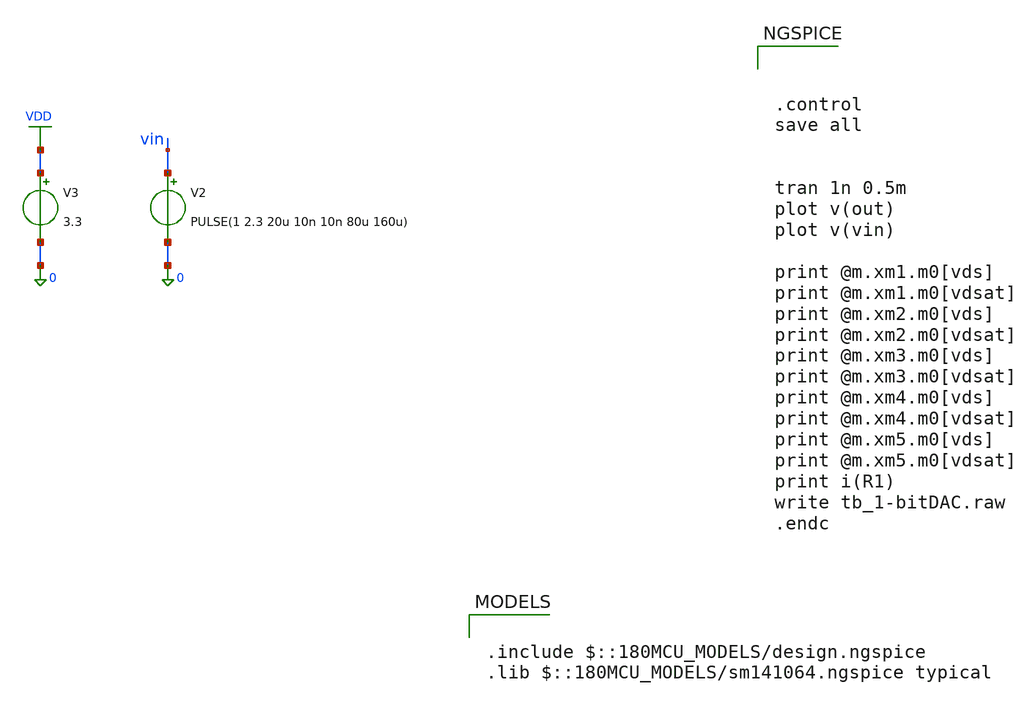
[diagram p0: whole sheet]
** sch_path: tb_1-bitDAC.sch
**.subckt tb_1-bitDAC
V2 vin 0 PULSE(1 2.3 20u 10n 10n 80u 160u)
V3 VDD 0 3.3
**** begin user architecture code

.include $::180MCU_MODELS/design.ngspice
.lib $::180MCU_MODELS/sm141064.ngspice typical




.control
save all


tran 1n 0.5m
plot v(out)
plot v(vin)

print @m.xm1.m0[vds]
print @m.xm1.m0[vdsat]
print @m.xm2.m0[vds]
print @m.xm2.m0[vdsat]
print @m.xm3.m0[vds]
print @m.xm3.m0[vdsat]
print @m.xm4.m0[vds]
print @m.xm4.m0[vdsat]
print @m.xm5.m0[vds]
print @m.xm5.m0[vdsat]
print i(R1)
write tb_1-bitDAC.raw
.endc


**** end user architecture code
**.ends
.GLOBAL VDD
.end
